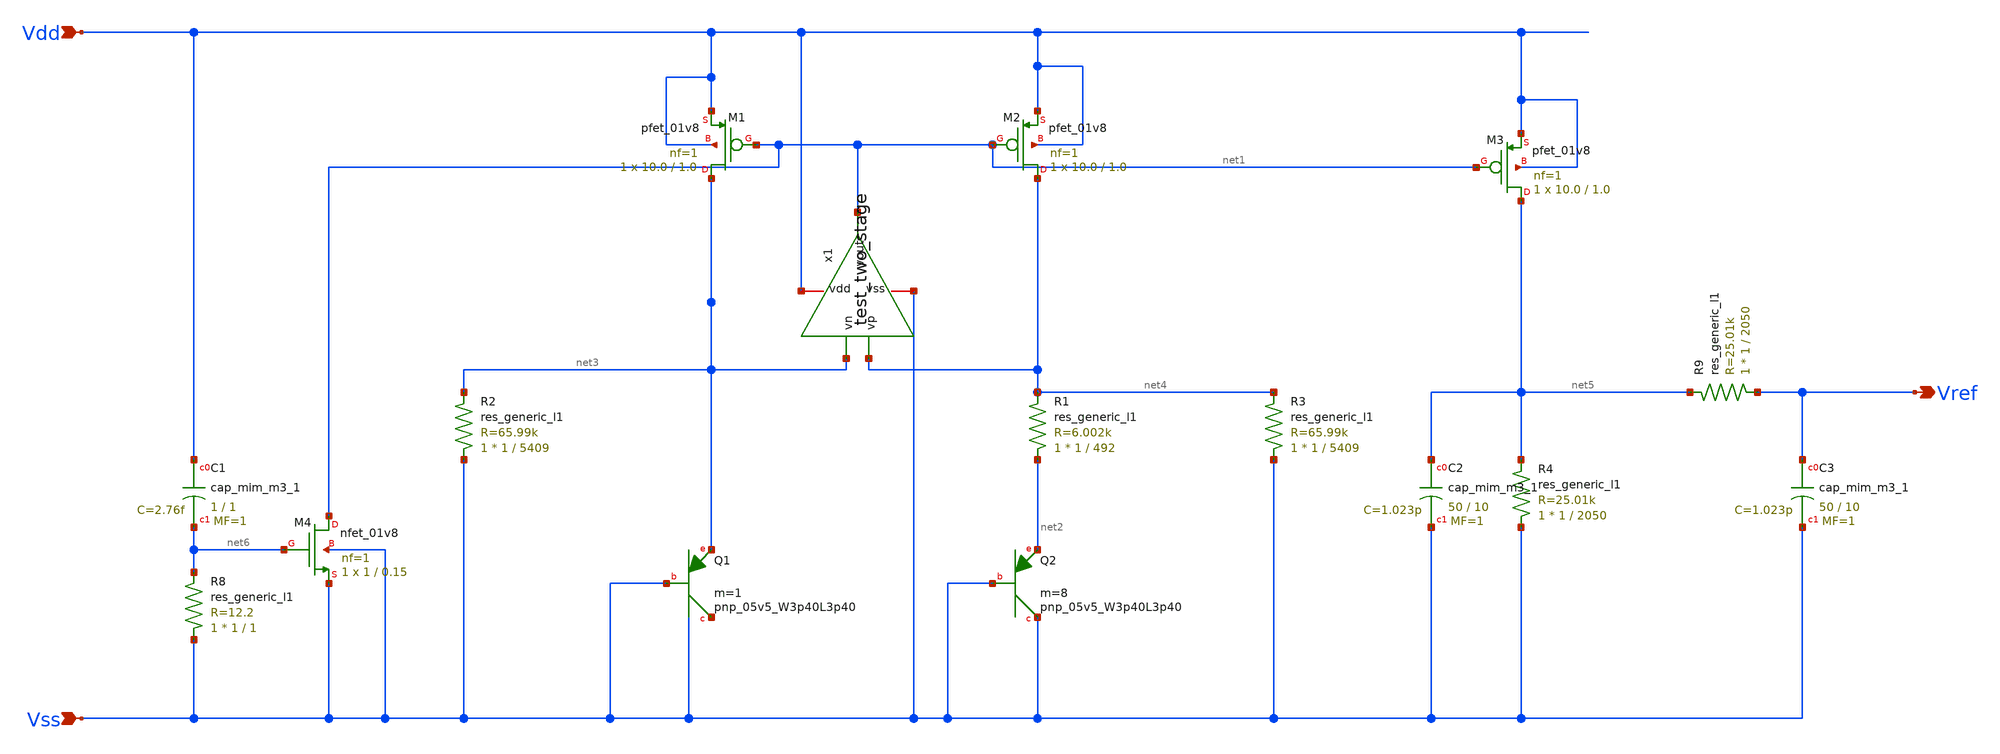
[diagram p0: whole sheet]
** sch_path: analog/library/LDO/bandgap.sch
**.subckt bandgap Vdd Vss Vref
*.ipin Vdd
*.ipin Vss
*.opin Vref
XM1 net3 net1 Vdd Vdd sky130_fd_pr__pfet_01v8 L=1.0 W=10.0 nf=1 ad='int((1 + 1)/2) * 10.0 / 1 * 0.29'
+ as='int((1 + 2)/2) * 10.0 / 1 * 0.29' pd='2*int((1 + 1)/2) * (10.0 / 1 + 0.29)' ps='2*int((1 + 2)/2) * (10.0 / 1 + 0.29)'
+ nrd='0.29 / 10.0 ' nrs='0.29 / 10.0 ' sa=0 sb=0 sd=0 mult=1 m=1
XM2 net4 net1 Vdd Vdd sky130_fd_pr__pfet_01v8 L=1.0 W=10.0 nf=1 ad='int((1 + 1)/2) * 10.0 / 1 * 0.29'
+ as='int((1 + 2)/2) * 10.0 / 1 * 0.29' pd='2*int((1 + 1)/2) * (10.0 / 1 + 0.29)' ps='2*int((1 + 2)/2) * (10.0 / 1 + 0.29)'
+ nrd='0.29 / 10.0 ' nrs='0.29 / 10.0 ' sa=0 sb=0 sd=0 mult=1 m=1
XQ1 net7 Vss net3 sky130_fd_pr__pnp_05v5_W3p40L3p40 m=1
XQ2 Vss Vss net2 sky130_fd_pr__pnp_05v5_W3p40L3p40 m=8
R1 net2 net4 sky130_fd_pr__res_generic_l1 W=1 L=492 m=1
R2 Vss net3 sky130_fd_pr__res_generic_l1 W=1 L=5409 m=1
R3 Vss net4 sky130_fd_pr__res_generic_l1 W=1 L=5409 m=1
XM3 net5 net1 Vdd Vdd sky130_fd_pr__pfet_01v8 L=1.0 W=10.0 nf=1 ad='int((1 + 1)/2) * 10.0 / 1 * 0.29'
+ as='int((1 + 2)/2) * 10.0 / 1 * 0.29' pd='2*int((1 + 1)/2) * (10.0 / 1 + 0.29)' ps='2*int((1 + 2)/2) * (10.0 / 1 + 0.29)'
+ nrd='0.29 / 10.0 ' nrs='0.29 / 10.0 ' sa=0 sb=0 sd=0 mult=1 m=1
R4 Vss net5 sky130_fd_pr__res_generic_l1 W=1 L=2050 m=1
XC1 Vdd net6 sky130_fd_pr__cap_mim_m3_1 W=1 L=1 MF=1 m=1
R8 Vss net6 sky130_fd_pr__res_generic_l1 W=1 L=1 m=1
XM4 net1 net6 Vss Vss sky130_fd_pr__nfet_01v8 L=0.15 W=1 nf=1 ad='int((1 + 1)/2) * 1 / 1 * 0.29' as='int((1 + 2)/2) * 1 / 1 * 0.29'
+ pd='2*int((1 + 1)/2) * (1 / 1 + 0.29)' ps='2*int((1 + 2)/2) * (1 / 1 + 0.29)' nrd='0.29 / 1 ' nrs='0.29 / 1 '
+ sa=0 sb=0 sd=0 mult=1 m=1
x1 Vdd net1 net3 net4 Vss test_two_stage
R9 Vref net5 sky130_fd_pr__res_generic_l1 W=1 L=2050 m=1
XC2 net5 Vss sky130_fd_pr__cap_mim_m3_1 W=50 L=10 MF=1 m=1
XC3 Vref Vss sky130_fd_pr__cap_mim_m3_1 W=50 L=10 MF=1 m=1
**.ends

* expanding   symbol:  test_two_stage.sym # of pins=5
** sym_path: analog/library/LDO/test_two_stage.sym
** sch_path: analog/library/LDO/test_two_stage.sch
.subckt test_two_stage vdd vout vn vp vss
*.iopin vdd
*.iopin vss
*.ipin vn
*.ipin vp
*.opin vout
XM1 net2 vn net1 vss sky130_fd_pr__nfet_01v8 L=3 W=18 nf=1 ad='int((nf+1)/2) * W/nf * 0.29' as='int((nf+2)/2) * W/nf * 0.29'
+ pd='2*int((nf+1)/2) * (W/nf + 0.29)' ps='2*int((nf+2)/2) * (W/nf + 0.29)' nrd='0.29 / W' nrs='0.29 / W'
+ sa=0 sb=0 sd=0 mult=1 m=1
XM2 net3 vp net1 vss sky130_fd_pr__nfet_01v8 L=3 W=18 nf=1 ad='int((nf+1)/2) * W/nf * 0.29' as='int((nf+2)/2) * W/nf * 0.29'
+ pd='2*int((nf+1)/2) * (W/nf + 0.29)' ps='2*int((nf+2)/2) * (W/nf + 0.29)' nrd='0.29 / W' nrs='0.29 / W'
+ sa=0 sb=0 sd=0 mult=1 m=1
XM4 net2 net2 vdd vdd sky130_fd_pr__pfet_01v8 L=3 W=30 nf=1 ad='int((nf+1)/2) * W/nf * 0.29' as='int((nf+2)/2) * W/nf * 0.29'
+ pd='2*int((nf+1)/2) * (W/nf + 0.29)' ps='2*int((nf+2)/2) * (W/nf + 0.29)' nrd='0.29 / W' nrs='0.29 / W'
+ sa=0 sb=0 sd=0 mult=1 m=1
XM5 net3 net2 vdd vdd sky130_fd_pr__pfet_01v8 L=3 W=30 nf=1 ad='int((nf+1)/2) * W/nf * 0.29' as='int((nf+2)/2) * W/nf * 0.29'
+ pd='2*int((nf+1)/2) * (W/nf + 0.29)' ps='2*int((nf+2)/2) * (W/nf + 0.29)' nrd='0.29 / W' nrs='0.29 / W'
+ sa=0 sb=0 sd=0 mult=1 m=1
XM6 vout net3 vdd vdd sky130_fd_pr__pfet_01v8 L=3 W=180 nf=1 ad='int((nf+1)/2) * W/nf * 0.29' as='int((nf+2)/2) * W/nf * 0.29'
+ pd='2*int((nf+1)/2) * (W/nf + 0.29)' ps='2*int((nf+2)/2) * (W/nf + 0.29)' nrd='0.29 / W' nrs='0.29 / W'
+ sa=0 sb=0 sd=0 mult=1 m=1
XM3 net1 vref vss vss sky130_fd_pr__nfet_01v8 L=1 W=1.8 nf=1 ad='int((nf+1)/2) * W/nf * 0.29' as='int((nf+2)/2) * W/nf * 0.29'
+ pd='2*int((nf+1)/2) * (W/nf + 0.29)' ps='2*int((nf+2)/2) * (W/nf + 0.29)' nrd='0.29 / W' nrs='0.29 / W'
+ sa=0 sb=0 sd=0 mult=1 m=1
XM8 vout vref vss vss sky130_fd_pr__nfet_01v8 L=1 W=5.4 nf=1 ad='int((nf+1)/2) * W/nf * 0.29' as='int((nf+2)/2) * W/nf * 0.29'
+ pd='2*int((nf+1)/2) * (W/nf + 0.29)' ps='2*int((nf+2)/2) * (W/nf + 0.29)' nrd='0.29 / W' nrs='0.29 / W'
+ sa=0 sb=0 sd=0 mult=1 m=1
XC1 net3 vout sky130_fd_pr__cap_mim_m3_1 W=50 L=10 MF=1 m=1
XM7 net4 net4 vdd vdd sky130_fd_pr__pfet_01v8 L=1 W=3 nf=1 ad='int((1 + 1)/2) * 3 / 1 * 0.29' as='int((1 + 2)/2) * 3 / 1 * 0.29'
+ pd='2*int((1 + 1)/2) * (3 / 1 + 0.29)' ps='2*int((1 + 2)/2) * (3 / 1 + 0.29)' nrd='0.29 / 3 ' nrs='0.29 / 3 '
+ sa=0 sb=0 sd=0 mult=1 m=1
XM9 vref net4 vdd vdd sky130_fd_pr__pfet_01v8 L=1 W=3 nf=1 ad='int((1 + 1)/2) * 3 / 1 * 0.29' as='int((1 + 2)/2) * 3 / 1 * 0.29'
+ pd='2*int((1 + 1)/2) * (3 / 1 + 0.29)' ps='2*int((1 + 2)/2) * (3 / 1 + 0.29)' nrd='0.29 / 3 ' nrs='0.29 / 3 '
+ sa=0 sb=0 sd=0 mult=1 m=1
XM10 net6 vref net5 vss sky130_fd_pr__nfet_01v8 L=1 W=8 nf=1 ad='int((1 + 1)/2) * 8 / 1 * 0.29' as='int((1 + 2)/2) * 8 / 1 * 0.29'
+ pd='2*int((1 + 1)/2) * (8 / 1 + 0.29)' ps='2*int((1 + 2)/2) * (8 / 1 + 0.29)' nrd='0.29 / 8 ' nrs='0.29 / 8 '
+ sa=0 sb=0 sd=0 mult=1 m=1
XM11 vref vref vss vss sky130_fd_pr__nfet_01v8 L=1 W=1 nf=1 ad='int((1 + 1)/2) * 1 / 1 * 0.29' as='int((1 + 2)/2) * 1 / 1 * 0.29'
+ pd='2*int((1 + 1)/2) * (1 / 1 + 0.29)' ps='2*int((1 + 2)/2) * (1 / 1 + 0.29)' nrd='0.29 / 1 ' nrs='0.29 / 1 '
+ sa=0 sb=0 sd=0 mult=1 m=1
R4 vss net5 sky130_fd_pr__res_generic_l1 W=1 L=1600 m=1
XM12 net4 vref net6 vss sky130_fd_pr__nfet_01v8 L=0.5 W=16 nf=1 ad='int((1 + 1)/2) * 16 / 1 * 0.29' as='int((1 + 2)/2) * 16 / 1 * 0.29'
+ pd='2*int((1 + 1)/2) * (16 / 1 + 0.29)' ps='2*int((1 + 2)/2) * (16 / 1 + 0.29)' nrd='0.29 / 16 ' nrs='0.29 / 16 '
+ sa=0 sb=0 sd=0 mult=1 m=1
.ends

.end
